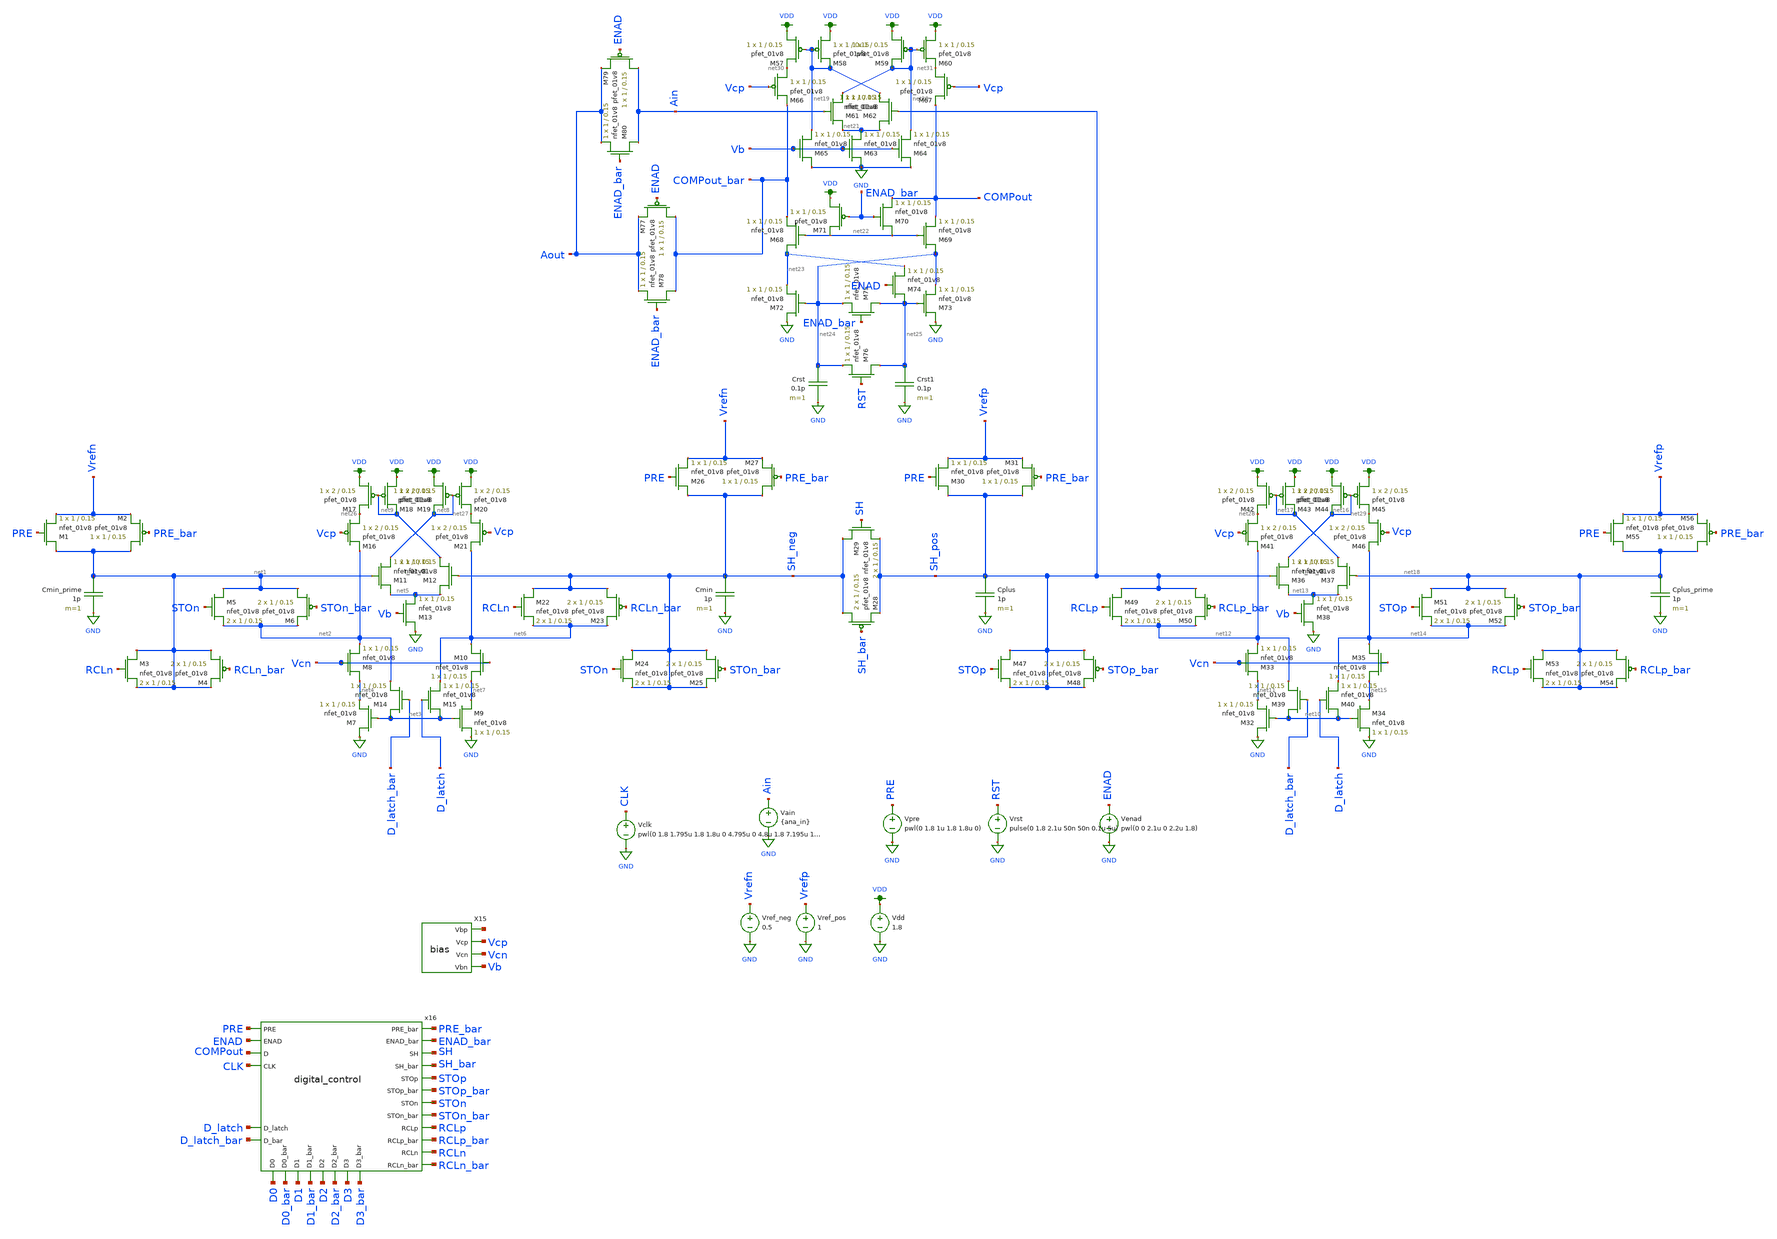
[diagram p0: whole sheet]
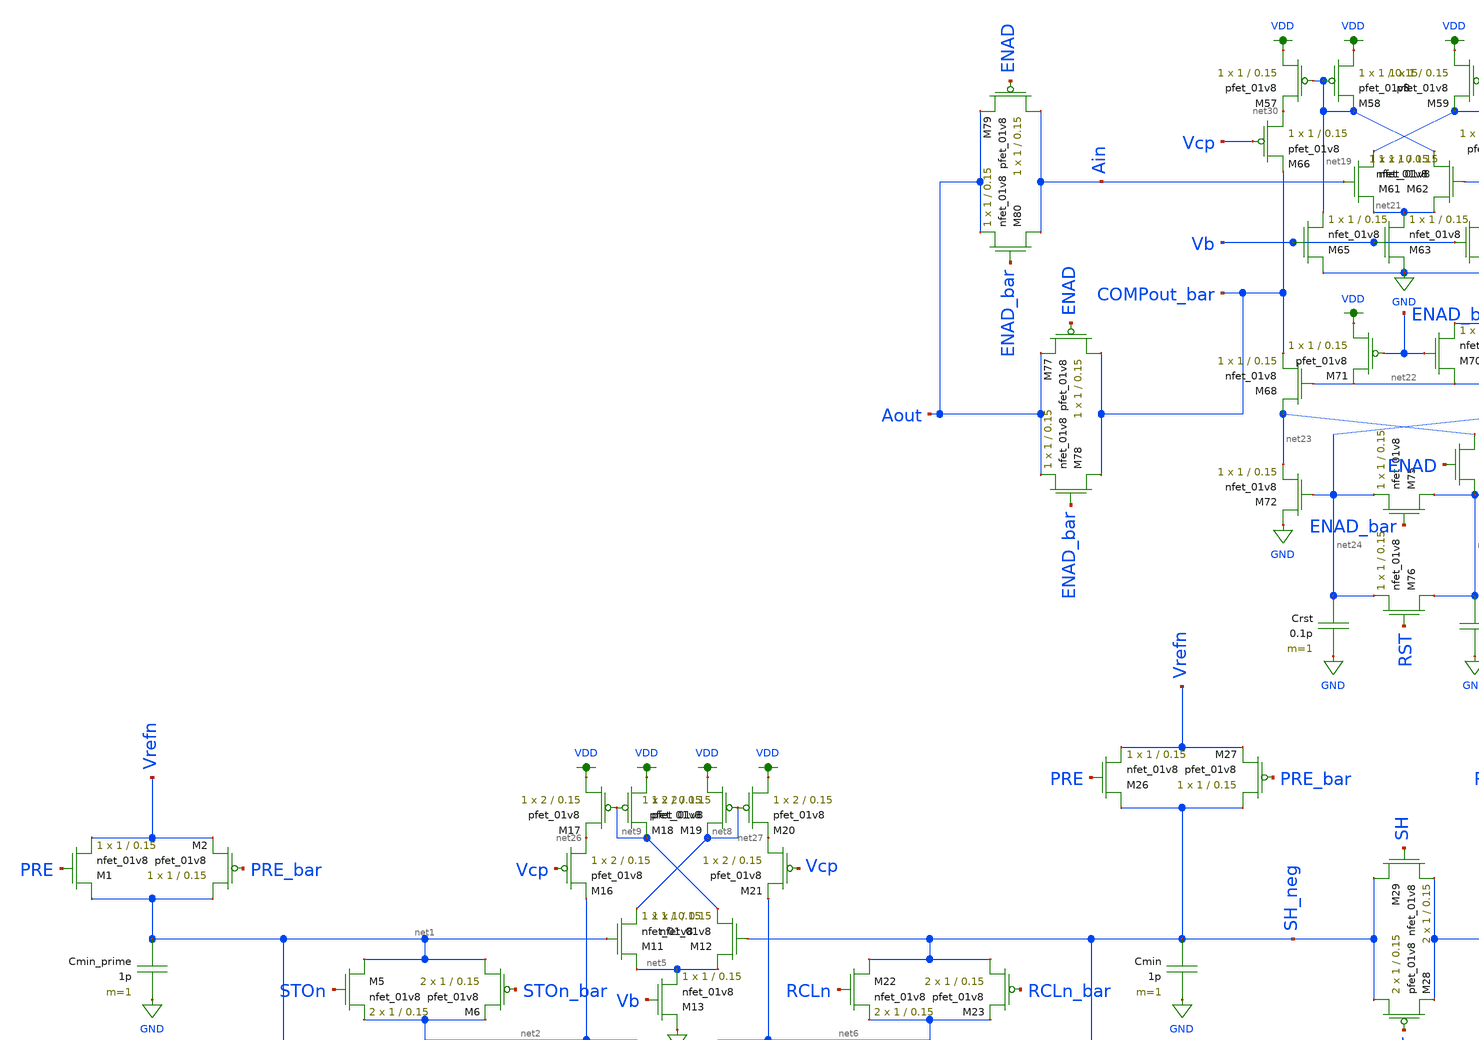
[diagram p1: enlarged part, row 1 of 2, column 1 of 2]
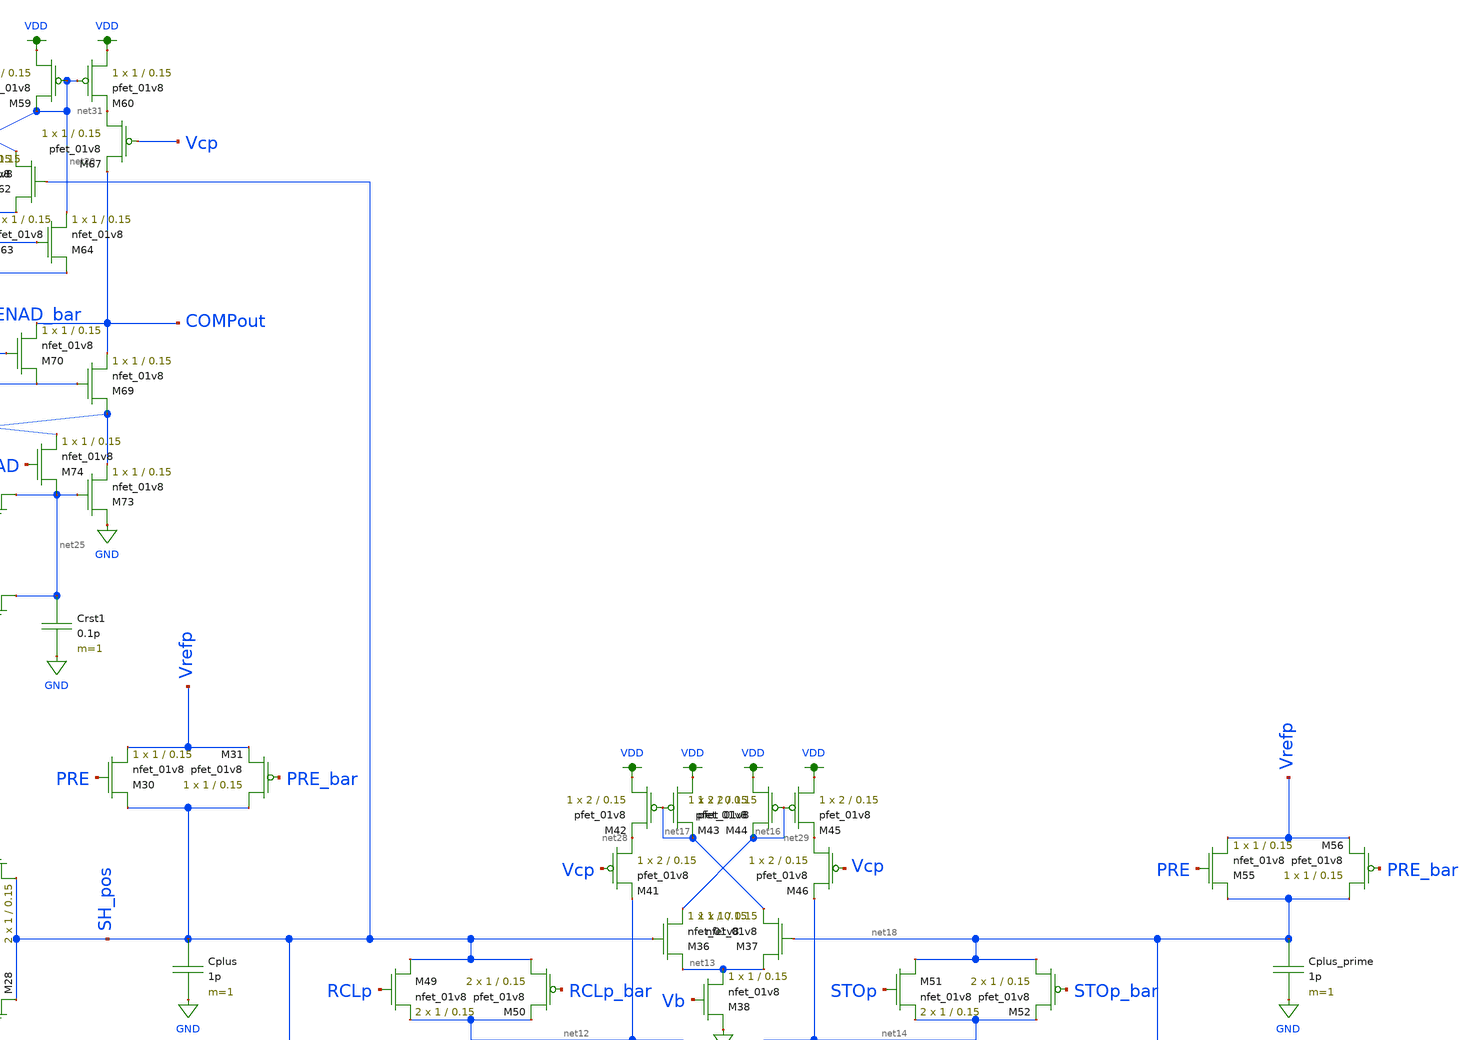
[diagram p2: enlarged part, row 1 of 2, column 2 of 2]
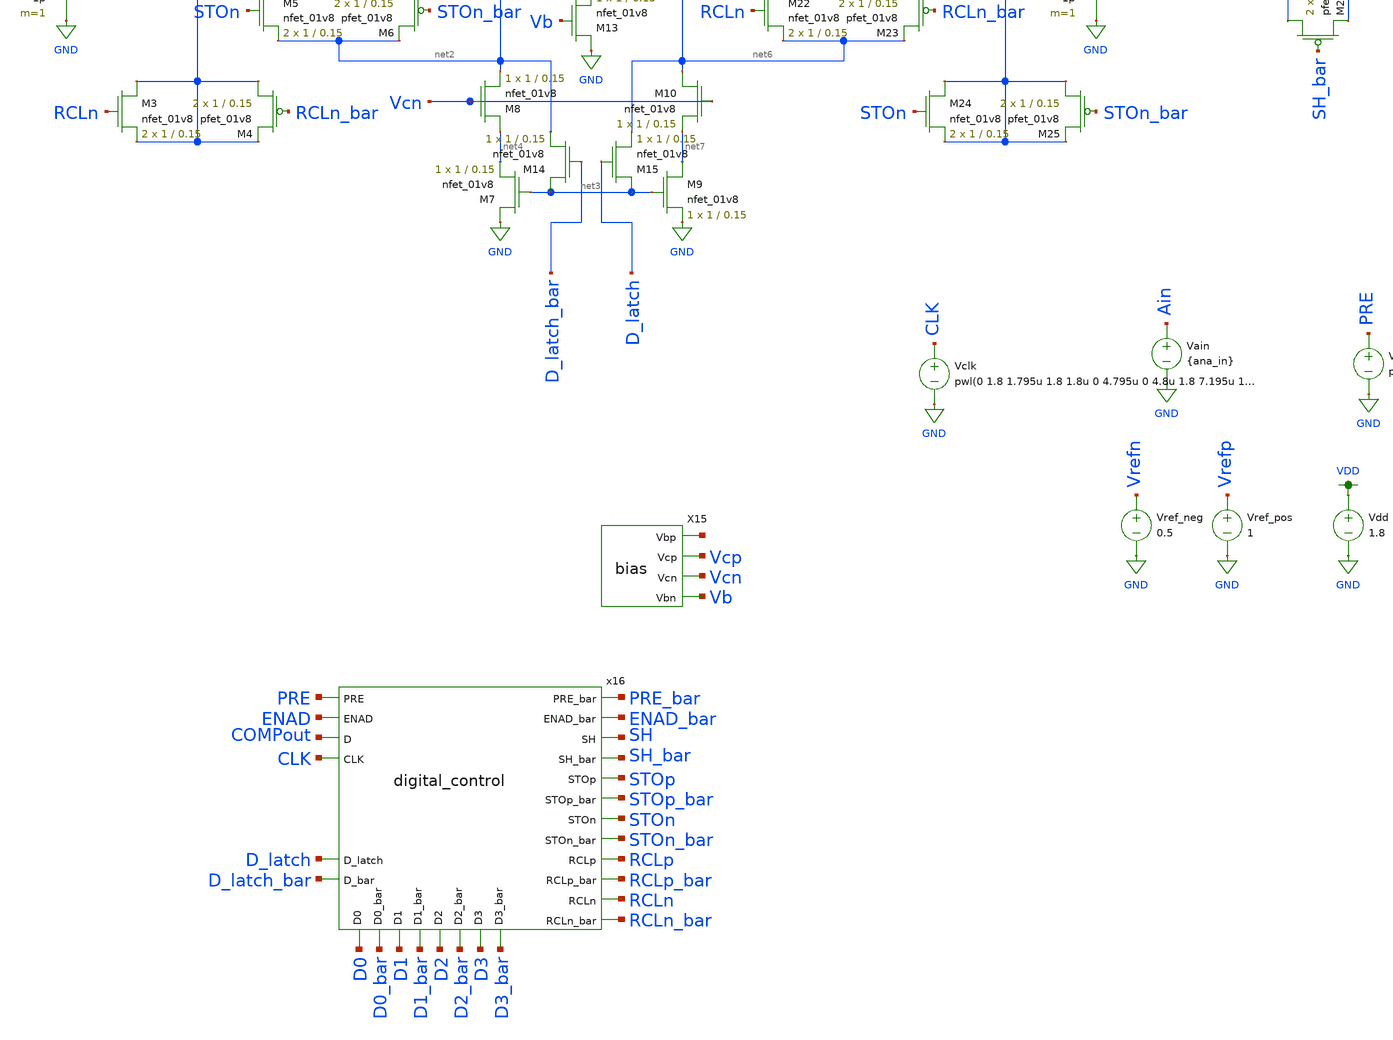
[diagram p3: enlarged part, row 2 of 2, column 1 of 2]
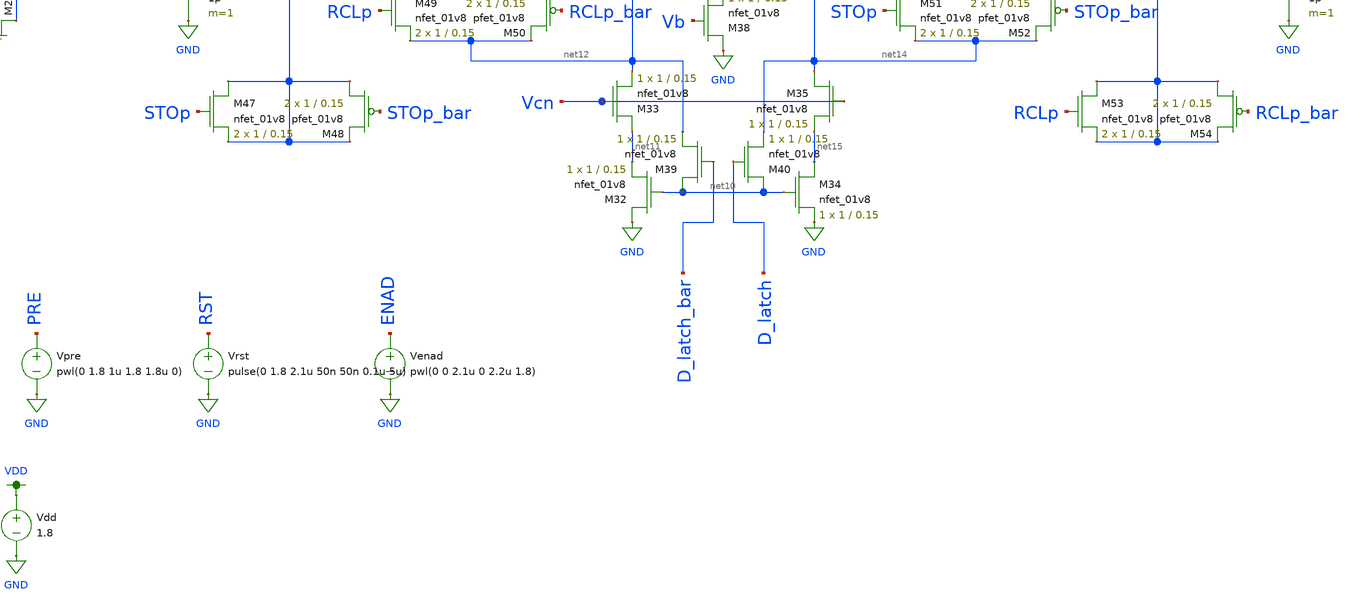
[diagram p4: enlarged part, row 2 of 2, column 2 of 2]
** sch_path: simulations/adc_mc.sch
**.subckt adc_mc
XM1 net1 PRE Vrefn GND sky130_fd_pr__nfet_01v8 L=0.15 W=1 nf=1 ad='int((nf+1)/2) * W/nf * 0.29' as='int((nf+2)/2) * W/nf * 0.29'
+ pd='2*int((nf+1)/2) * (W/nf + 0.29)' ps='2*int((nf+2)/2) * (W/nf + 0.29)' nrd='0.29 / W' nrs='0.29 / W'
+ sa=0 sb=0 sd=0 mult=1 m=1
XM2 net1 PRE_bar Vrefn VDD sky130_fd_pr__pfet_01v8 L=0.15 W=1 nf=1 ad='int((nf+1)/2) * W/nf * 0.29' as='int((nf+2)/2) * W/nf * 0.29'
+ pd='2*int((nf+1)/2) * (W/nf + 0.29)' ps='2*int((nf+2)/2) * (W/nf + 0.29)' nrd='0.29 / W' nrs='0.29 / W'
+ sa=0 sb=0 sd=0 mult=1 m=1
Cmin_prime net1 GND 1p m=1
XM3 net1 RCLn net1 GND sky130_fd_pr__nfet_01v8 L=0.15 W=1 nf=1 ad='int((nf+1)/2) * W/nf * 0.29' as='int((nf+2)/2) * W/nf * 0.29'
+ pd='2*int((nf+1)/2) * (W/nf + 0.29)' ps='2*int((nf+2)/2) * (W/nf + 0.29)' nrd='0.29 / W' nrs='0.29 / W'
+ sa=0 sb=0 sd=0 mult=2 m=2
XM4 net1 RCLn_bar net1 VDD sky130_fd_pr__pfet_01v8 L=0.15 W=1 nf=1 ad='int((nf+1)/2) * W/nf * 0.29' as='int((nf+2)/2) * W/nf * 0.29'
+ pd='2*int((nf+1)/2) * (W/nf + 0.29)' ps='2*int((nf+2)/2) * (W/nf + 0.29)' nrd='0.29 / W' nrs='0.29 / W'
+ sa=0 sb=0 sd=0 mult=2 m=2
XM5 net1 STOn net2 GND sky130_fd_pr__nfet_01v8 L=0.15 W=1 nf=1 ad='int((nf+1)/2) * W/nf * 0.29' as='int((nf+2)/2) * W/nf * 0.29'
+ pd='2*int((nf+1)/2) * (W/nf + 0.29)' ps='2*int((nf+2)/2) * (W/nf + 0.29)' nrd='0.29 / W' nrs='0.29 / W'
+ sa=0 sb=0 sd=0 mult=2 m=2
XM6 net1 STOn_bar net2 VDD sky130_fd_pr__pfet_01v8 L=0.15 W=1 nf=1 ad='int((nf+1)/2) * W/nf * 0.29' as='int((nf+2)/2) * W/nf * 0.29'
+ pd='2*int((nf+1)/2) * (W/nf + 0.29)' ps='2*int((nf+2)/2) * (W/nf + 0.29)' nrd='0.29 / W' nrs='0.29 / W'
+ sa=0 sb=0 sd=0 mult=2 m=2
XM7 GND net3 net4 GND sky130_fd_pr__nfet_01v8 L=0.15 W=1 nf=1 ad='int((nf+1)/2) * W/nf * 0.29' as='int((nf+2)/2) * W/nf * 0.29'
+ pd='2*int((nf+1)/2) * (W/nf + 0.29)' ps='2*int((nf+2)/2) * (W/nf + 0.29)' nrd='0.29 / W' nrs='0.29 / W'
+ sa=0 sb=0 sd=0 mult=1 m=1
XM8 net4 Vcn net2 GND sky130_fd_pr__nfet_01v8 L=0.15 W=1 nf=1 ad='int((nf+1)/2) * W/nf * 0.29' as='int((nf+2)/2) * W/nf * 0.29'
+ pd='2*int((nf+1)/2) * (W/nf + 0.29)' ps='2*int((nf+2)/2) * (W/nf + 0.29)' nrd='0.29 / W' nrs='0.29 / W'
+ sa=0 sb=0 sd=0 mult=1 m=1
XM9 net7 net3 GND GND sky130_fd_pr__nfet_01v8 L=0.15 W=1 nf=1 ad='int((nf+1)/2) * W/nf * 0.29' as='int((nf+2)/2) * W/nf * 0.29'
+ pd='2*int((nf+1)/2) * (W/nf + 0.29)' ps='2*int((nf+2)/2) * (W/nf + 0.29)' nrd='0.29 / W' nrs='0.29 / W'
+ sa=0 sb=0 sd=0 mult=1 m=1
XM10 net6 Vcn net7 GND sky130_fd_pr__nfet_01v8 L=0.15 W=1 nf=1 ad='int((nf+1)/2) * W/nf * 0.29' as='int((nf+2)/2) * W/nf * 0.29'
+ pd='2*int((nf+1)/2) * (W/nf + 0.29)' ps='2*int((nf+2)/2) * (W/nf + 0.29)' nrd='0.29 / W' nrs='0.29 / W'
+ sa=0 sb=0 sd=0 mult=1 m=1
XM11 net5 net1 net8 GND sky130_fd_pr__nfet_01v8 L=0.15 W=1 nf=1 ad='int((nf+1)/2) * W/nf * 0.29' as='int((nf+2)/2) * W/nf * 0.29'
+ pd='2*int((nf+1)/2) * (W/nf + 0.29)' ps='2*int((nf+2)/2) * (W/nf + 0.29)' nrd='0.29 / W' nrs='0.29 / W'
+ sa=0 sb=0 sd=0 mult=1 m=1
XM12 net5 SH_neg net9 GND sky130_fd_pr__nfet_01v8 L=0.15 W=1 nf=1 ad='int((nf+1)/2) * W/nf * 0.29' as='int((nf+2)/2) * W/nf * 0.29'
+ pd='2*int((nf+1)/2) * (W/nf + 0.29)' ps='2*int((nf+2)/2) * (W/nf + 0.29)' nrd='0.29 / W' nrs='0.29 / W'
+ sa=0 sb=0 sd=0 mult=1 m=1
XM13 GND Vb net5 GND sky130_fd_pr__nfet_01v8 L=0.15 W=1 nf=1 ad='int((nf+1)/2) * W/nf * 0.29' as='int((nf+2)/2) * W/nf * 0.29'
+ pd='2*int((nf+1)/2) * (W/nf + 0.29)' ps='2*int((nf+2)/2) * (W/nf + 0.29)' nrd='0.29 / W' nrs='0.29 / W'
+ sa=0 sb=0 sd=0 mult=1 m=1
XM14 net3 D_latch_bar net2 GND sky130_fd_pr__nfet_01v8 L=0.15 W=1 nf=1 ad='int((nf+1)/2) * W/nf * 0.29'
+ as='int((nf+2)/2) * W/nf * 0.29' pd='2*int((nf+1)/2) * (W/nf + 0.29)' ps='2*int((nf+2)/2) * (W/nf + 0.29)'
+ nrd='0.29 / W' nrs='0.29 / W' sa=0 sb=0 sd=0 mult=1 m=1
XM15 net3 D_latch net6 GND sky130_fd_pr__nfet_01v8 L=0.15 W=1 nf=1 ad='int((nf+1)/2) * W/nf * 0.29' as='int((nf+2)/2) * W/nf * 0.29'
+ pd='2*int((nf+1)/2) * (W/nf + 0.29)' ps='2*int((nf+2)/2) * (W/nf + 0.29)' nrd='0.29 / W' nrs='0.29 / W'
+ sa=0 sb=0 sd=0 mult=1 m=1
XM16 net26 Vcp net2 VDD sky130_fd_pr__pfet_01v8 L=0.15 W=2 nf=1 ad='int((nf+1)/2) * W/nf * 0.29' as='int((nf+2)/2) * W/nf * 0.29'
+ pd='2*int((nf+1)/2) * (W/nf + 0.29)' ps='2*int((nf+2)/2) * (W/nf + 0.29)' nrd='0.29 / W' nrs='0.29 / W'
+ sa=0 sb=0 sd=0 mult=1 m=1
XM17 VDD net9 net26 VDD sky130_fd_pr__pfet_01v8 L=0.15 W=2 nf=1 ad='int((nf+1)/2) * W/nf * 0.29' as='int((nf+2)/2) * W/nf * 0.29'
+ pd='2*int((nf+1)/2) * (W/nf + 0.29)' ps='2*int((nf+2)/2) * (W/nf + 0.29)' nrd='0.29 / W' nrs='0.29 / W'
+ sa=0 sb=0 sd=0 mult=1 m=1
XM18 VDD net9 net9 VDD sky130_fd_pr__pfet_01v8 L=0.15 W=2 nf=1 ad='int((nf+1)/2) * W/nf * 0.29' as='int((nf+2)/2) * W/nf * 0.29'
+ pd='2*int((nf+1)/2) * (W/nf + 0.29)' ps='2*int((nf+2)/2) * (W/nf + 0.29)' nrd='0.29 / W' nrs='0.29 / W'
+ sa=0 sb=0 sd=0 mult=1 m=1
XM19 VDD net8 net8 VDD sky130_fd_pr__pfet_01v8 L=0.15 W=2 nf=1 ad='int((nf+1)/2) * W/nf * 0.29' as='int((nf+2)/2) * W/nf * 0.29'
+ pd='2*int((nf+1)/2) * (W/nf + 0.29)' ps='2*int((nf+2)/2) * (W/nf + 0.29)' nrd='0.29 / W' nrs='0.29 / W'
+ sa=0 sb=0 sd=0 mult=1 m=1
XM20 VDD net8 net27 VDD sky130_fd_pr__pfet_01v8 L=0.15 W=2 nf=1 ad='int((nf+1)/2) * W/nf * 0.29' as='int((nf+2)/2) * W/nf * 0.29'
+ pd='2*int((nf+1)/2) * (W/nf + 0.29)' ps='2*int((nf+2)/2) * (W/nf + 0.29)' nrd='0.29 / W' nrs='0.29 / W'
+ sa=0 sb=0 sd=0 mult=1 m=1
XM21 net27 Vcp net6 VDD sky130_fd_pr__pfet_01v8 L=0.15 W=2 nf=1 ad='int((nf+1)/2) * W/nf * 0.29' as='int((nf+2)/2) * W/nf * 0.29'
+ pd='2*int((nf+1)/2) * (W/nf + 0.29)' ps='2*int((nf+2)/2) * (W/nf + 0.29)' nrd='0.29 / W' nrs='0.29 / W'
+ sa=0 sb=0 sd=0 mult=1 m=1
XM22 SH_neg RCLn net6 GND sky130_fd_pr__nfet_01v8 L=0.15 W=1 nf=1 ad='int((nf+1)/2) * W/nf * 0.29' as='int((nf+2)/2) * W/nf * 0.29'
+ pd='2*int((nf+1)/2) * (W/nf + 0.29)' ps='2*int((nf+2)/2) * (W/nf + 0.29)' nrd='0.29 / W' nrs='0.29 / W'
+ sa=0 sb=0 sd=0 mult=2 m=2
XM23 SH_neg RCLn_bar net6 VDD sky130_fd_pr__pfet_01v8 L=0.15 W=1 nf=1 ad='int((nf+1)/2) * W/nf * 0.29'
+ as='int((nf+2)/2) * W/nf * 0.29' pd='2*int((nf+1)/2) * (W/nf + 0.29)' ps='2*int((nf+2)/2) * (W/nf + 0.29)'
+ nrd='0.29 / W' nrs='0.29 / W' sa=0 sb=0 sd=0 mult=2 m=2
XM24 SH_neg STOn SH_neg GND sky130_fd_pr__nfet_01v8 L=0.15 W=1 nf=1 ad='int((nf+1)/2) * W/nf * 0.29'
+ as='int((nf+2)/2) * W/nf * 0.29' pd='2*int((nf+1)/2) * (W/nf + 0.29)' ps='2*int((nf+2)/2) * (W/nf + 0.29)'
+ nrd='0.29 / W' nrs='0.29 / W' sa=0 sb=0 sd=0 mult=2 m=2
XM25 SH_neg STOn_bar SH_neg VDD sky130_fd_pr__pfet_01v8 L=0.15 W=1 nf=1 ad='int((nf+1)/2) * W/nf * 0.29'
+ as='int((nf+2)/2) * W/nf * 0.29' pd='2*int((nf+1)/2) * (W/nf + 0.29)' ps='2*int((nf+2)/2) * (W/nf + 0.29)'
+ nrd='0.29 / W' nrs='0.29 / W' sa=0 sb=0 sd=0 mult=2 m=2
XM26 SH_neg PRE Vrefn GND sky130_fd_pr__nfet_01v8 L=0.15 W=1 nf=1 ad='int((nf+1)/2) * W/nf * 0.29' as='int((nf+2)/2) * W/nf * 0.29'
+ pd='2*int((nf+1)/2) * (W/nf + 0.29)' ps='2*int((nf+2)/2) * (W/nf + 0.29)' nrd='0.29 / W' nrs='0.29 / W'
+ sa=0 sb=0 sd=0 mult=1 m=1
XM27 SH_neg PRE_bar Vrefn VDD sky130_fd_pr__pfet_01v8 L=0.15 W=1 nf=1 ad='int((nf+1)/2) * W/nf * 0.29'
+ as='int((nf+2)/2) * W/nf * 0.29' pd='2*int((nf+1)/2) * (W/nf + 0.29)' ps='2*int((nf+2)/2) * (W/nf + 0.29)'
+ nrd='0.29 / W' nrs='0.29 / W' sa=0 sb=0 sd=0 mult=1 m=1
Cmin SH_neg GND 1p m=1
XM28 SH_neg SH_bar SH_pos VDD sky130_fd_pr__pfet_01v8 L=0.15 W=1 nf=1 ad='int((nf+1)/2) * W/nf * 0.29'
+ as='int((nf+2)/2) * W/nf * 0.29' pd='2*int((nf+1)/2) * (W/nf + 0.29)' ps='2*int((nf+2)/2) * (W/nf + 0.29)'
+ nrd='0.29 / W' nrs='0.29 / W' sa=0 sb=0 sd=0 mult=2 m=2
XM29 SH_neg SH SH_pos GND sky130_fd_pr__nfet_01v8 L=0.15 W=1 nf=1 ad='int((nf+1)/2) * W/nf * 0.29' as='int((nf+2)/2) * W/nf * 0.29'
+ pd='2*int((nf+1)/2) * (W/nf + 0.29)' ps='2*int((nf+2)/2) * (W/nf + 0.29)' nrd='0.29 / W' nrs='0.29 / W'
+ sa=0 sb=0 sd=0 mult=2 m=2
XM30 SH_pos PRE Vrefp GND sky130_fd_pr__nfet_01v8 L=0.15 W=1 nf=1 ad='int((nf+1)/2) * W/nf * 0.29' as='int((nf+2)/2) * W/nf * 0.29'
+ pd='2*int((nf+1)/2) * (W/nf + 0.29)' ps='2*int((nf+2)/2) * (W/nf + 0.29)' nrd='0.29 / W' nrs='0.29 / W'
+ sa=0 sb=0 sd=0 mult=1 m=1
XM31 SH_pos PRE_bar Vrefp VDD sky130_fd_pr__pfet_01v8 L=0.15 W=1 nf=1 ad='int((nf+1)/2) * W/nf * 0.29'
+ as='int((nf+2)/2) * W/nf * 0.29' pd='2*int((nf+1)/2) * (W/nf + 0.29)' ps='2*int((nf+2)/2) * (W/nf + 0.29)'
+ nrd='0.29 / W' nrs='0.29 / W' sa=0 sb=0 sd=0 mult=1 m=1
Cplus SH_pos GND 1p m=1
XM32 GND net10 net11 GND sky130_fd_pr__nfet_01v8 L=0.15 W=1 nf=1 ad='int((nf+1)/2) * W/nf * 0.29' as='int((nf+2)/2) * W/nf * 0.29'
+ pd='2*int((nf+1)/2) * (W/nf + 0.29)' ps='2*int((nf+2)/2) * (W/nf + 0.29)' nrd='0.29 / W' nrs='0.29 / W'
+ sa=0 sb=0 sd=0 mult=1 m=1
XM33 net11 Vcn net12 GND sky130_fd_pr__nfet_01v8 L=0.15 W=1 nf=1 ad='int((nf+1)/2) * W/nf * 0.29' as='int((nf+2)/2) * W/nf * 0.29'
+ pd='2*int((nf+1)/2) * (W/nf + 0.29)' ps='2*int((nf+2)/2) * (W/nf + 0.29)' nrd='0.29 / W' nrs='0.29 / W'
+ sa=0 sb=0 sd=0 mult=1 m=1
XM34 net15 net10 GND GND sky130_fd_pr__nfet_01v8 L=0.15 W=1 nf=1 ad='int((nf+1)/2) * W/nf * 0.29' as='int((nf+2)/2) * W/nf * 0.29'
+ pd='2*int((nf+1)/2) * (W/nf + 0.29)' ps='2*int((nf+2)/2) * (W/nf + 0.29)' nrd='0.29 / W' nrs='0.29 / W'
+ sa=0 sb=0 sd=0 mult=1 m=1
XM35 net14 Vcn net15 GND sky130_fd_pr__nfet_01v8 L=0.15 W=1 nf=1 ad='int((nf+1)/2) * W/nf * 0.29' as='int((nf+2)/2) * W/nf * 0.29'
+ pd='2*int((nf+1)/2) * (W/nf + 0.29)' ps='2*int((nf+2)/2) * (W/nf + 0.29)' nrd='0.29 / W' nrs='0.29 / W'
+ sa=0 sb=0 sd=0 mult=1 m=1
XM36 net13 SH_pos net16 GND sky130_fd_pr__nfet_01v8 L=0.15 W=1 nf=1 ad='int((nf+1)/2) * W/nf * 0.29'
+ as='int((nf+2)/2) * W/nf * 0.29' pd='2*int((nf+1)/2) * (W/nf + 0.29)' ps='2*int((nf+2)/2) * (W/nf + 0.29)'
+ nrd='0.29 / W' nrs='0.29 / W' sa=0 sb=0 sd=0 mult=1 m=1
XM37 net13 net18 net17 GND sky130_fd_pr__nfet_01v8 L=0.15 W=1 nf=1 ad='int((nf+1)/2) * W/nf * 0.29' as='int((nf+2)/2) * W/nf * 0.29'
+ pd='2*int((nf+1)/2) * (W/nf + 0.29)' ps='2*int((nf+2)/2) * (W/nf + 0.29)' nrd='0.29 / W' nrs='0.29 / W'
+ sa=0 sb=0 sd=0 mult=1 m=1
XM38 GND Vb net13 GND sky130_fd_pr__nfet_01v8 L=0.15 W=1 nf=1 ad='int((nf+1)/2) * W/nf * 0.29' as='int((nf+2)/2) * W/nf * 0.29'
+ pd='2*int((nf+1)/2) * (W/nf + 0.29)' ps='2*int((nf+2)/2) * (W/nf + 0.29)' nrd='0.29 / W' nrs='0.29 / W'
+ sa=0 sb=0 sd=0 mult=1 m=1
XM39 net10 D_latch_bar net12 GND sky130_fd_pr__nfet_01v8 L=0.15 W=1 nf=1 ad='int((nf+1)/2) * W/nf * 0.29'
+ as='int((nf+2)/2) * W/nf * 0.29' pd='2*int((nf+1)/2) * (W/nf + 0.29)' ps='2*int((nf+2)/2) * (W/nf + 0.29)'
+ nrd='0.29 / W' nrs='0.29 / W' sa=0 sb=0 sd=0 mult=1 m=1
XM40 net10 D_latch net14 GND sky130_fd_pr__nfet_01v8 L=0.15 W=1 nf=1 ad='int((nf+1)/2) * W/nf * 0.29'
+ as='int((nf+2)/2) * W/nf * 0.29' pd='2*int((nf+1)/2) * (W/nf + 0.29)' ps='2*int((nf+2)/2) * (W/nf + 0.29)'
+ nrd='0.29 / W' nrs='0.29 / W' sa=0 sb=0 sd=0 mult=1 m=1
XM41 net28 Vcp net12 VDD sky130_fd_pr__pfet_01v8 L=0.15 W=2 nf=1 ad='int((nf+1)/2) * W/nf * 0.29' as='int((nf+2)/2) * W/nf * 0.29'
+ pd='2*int((nf+1)/2) * (W/nf + 0.29)' ps='2*int((nf+2)/2) * (W/nf + 0.29)' nrd='0.29 / W' nrs='0.29 / W'
+ sa=0 sb=0 sd=0 mult=1 m=1
XM42 VDD net17 net28 VDD sky130_fd_pr__pfet_01v8 L=0.15 W=2 nf=1 ad='int((nf+1)/2) * W/nf * 0.29' as='int((nf+2)/2) * W/nf * 0.29'
+ pd='2*int((nf+1)/2) * (W/nf + 0.29)' ps='2*int((nf+2)/2) * (W/nf + 0.29)' nrd='0.29 / W' nrs='0.29 / W'
+ sa=0 sb=0 sd=0 mult=1 m=1
XM43 VDD net17 net17 VDD sky130_fd_pr__pfet_01v8 L=0.15 W=2 nf=1 ad='int((nf+1)/2) * W/nf * 0.29' as='int((nf+2)/2) * W/nf * 0.29'
+ pd='2*int((nf+1)/2) * (W/nf + 0.29)' ps='2*int((nf+2)/2) * (W/nf + 0.29)' nrd='0.29 / W' nrs='0.29 / W'
+ sa=0 sb=0 sd=0 mult=1 m=1
XM44 VDD net16 net16 VDD sky130_fd_pr__pfet_01v8 L=0.15 W=2 nf=1 ad='int((nf+1)/2) * W/nf * 0.29' as='int((nf+2)/2) * W/nf * 0.29'
+ pd='2*int((nf+1)/2) * (W/nf + 0.29)' ps='2*int((nf+2)/2) * (W/nf + 0.29)' nrd='0.29 / W' nrs='0.29 / W'
+ sa=0 sb=0 sd=0 mult=1 m=1
XM45 VDD net16 net29 VDD sky130_fd_pr__pfet_01v8 L=0.15 W=2 nf=1 ad='int((nf+1)/2) * W/nf * 0.29' as='int((nf+2)/2) * W/nf * 0.29'
+ pd='2*int((nf+1)/2) * (W/nf + 0.29)' ps='2*int((nf+2)/2) * (W/nf + 0.29)' nrd='0.29 / W' nrs='0.29 / W'
+ sa=0 sb=0 sd=0 mult=1 m=1
XM46 net29 Vcp net14 VDD sky130_fd_pr__pfet_01v8 L=0.15 W=2 nf=1 ad='int((nf+1)/2) * W/nf * 0.29' as='int((nf+2)/2) * W/nf * 0.29'
+ pd='2*int((nf+1)/2) * (W/nf + 0.29)' ps='2*int((nf+2)/2) * (W/nf + 0.29)' nrd='0.29 / W' nrs='0.29 / W'
+ sa=0 sb=0 sd=0 mult=1 m=1
XM47 SH_pos STOp SH_pos GND sky130_fd_pr__nfet_01v8 L=0.15 W=1 nf=1 ad='int((nf+1)/2) * W/nf * 0.29'
+ as='int((nf+2)/2) * W/nf * 0.29' pd='2*int((nf+1)/2) * (W/nf + 0.29)' ps='2*int((nf+2)/2) * (W/nf + 0.29)'
+ nrd='0.29 / W' nrs='0.29 / W' sa=0 sb=0 sd=0 mult=2 m=2
XM48 SH_pos STOp_bar SH_pos VDD sky130_fd_pr__pfet_01v8 L=0.15 W=1 nf=1 ad='int((nf+1)/2) * W/nf * 0.29'
+ as='int((nf+2)/2) * W/nf * 0.29' pd='2*int((nf+1)/2) * (W/nf + 0.29)' ps='2*int((nf+2)/2) * (W/nf + 0.29)'
+ nrd='0.29 / W' nrs='0.29 / W' sa=0 sb=0 sd=0 mult=2 m=2
XM49 SH_pos RCLp net12 GND sky130_fd_pr__nfet_01v8 L=0.15 W=1 nf=1 ad='int((nf+1)/2) * W/nf * 0.29' as='int((nf+2)/2) * W/nf * 0.29'
+ pd='2*int((nf+1)/2) * (W/nf + 0.29)' ps='2*int((nf+2)/2) * (W/nf + 0.29)' nrd='0.29 / W' nrs='0.29 / W'
+ sa=0 sb=0 sd=0 mult=2 m=2
XM50 SH_pos RCLp_bar net12 VDD sky130_fd_pr__pfet_01v8 L=0.15 W=1 nf=1 ad='int((nf+1)/2) * W/nf * 0.29'
+ as='int((nf+2)/2) * W/nf * 0.29' pd='2*int((nf+1)/2) * (W/nf + 0.29)' ps='2*int((nf+2)/2) * (W/nf + 0.29)'
+ nrd='0.29 / W' nrs='0.29 / W' sa=0 sb=0 sd=0 mult=2 m=2
XM51 net18 STOp net14 GND sky130_fd_pr__nfet_01v8 L=0.15 W=1 nf=1 ad='int((nf+1)/2) * W/nf * 0.29' as='int((nf+2)/2) * W/nf * 0.29'
+ pd='2*int((nf+1)/2) * (W/nf + 0.29)' ps='2*int((nf+2)/2) * (W/nf + 0.29)' nrd='0.29 / W' nrs='0.29 / W'
+ sa=0 sb=0 sd=0 mult=2 m=2
XM52 net18 STOp_bar net14 VDD sky130_fd_pr__pfet_01v8 L=0.15 W=1 nf=1 ad='int((nf+1)/2) * W/nf * 0.29'
+ as='int((nf+2)/2) * W/nf * 0.29' pd='2*int((nf+1)/2) * (W/nf + 0.29)' ps='2*int((nf+2)/2) * (W/nf + 0.29)'
+ nrd='0.29 / W' nrs='0.29 / W' sa=0 sb=0 sd=0 mult=2 m=2
XM53 net18 RCLp net18 GND sky130_fd_pr__nfet_01v8 L=0.15 W=1 nf=1 ad='int((nf+1)/2) * W/nf * 0.29' as='int((nf+2)/2) * W/nf * 0.29'
+ pd='2*int((nf+1)/2) * (W/nf + 0.29)' ps='2*int((nf+2)/2) * (W/nf + 0.29)' nrd='0.29 / W' nrs='0.29 / W'
+ sa=0 sb=0 sd=0 mult=2 m=2
XM54 net18 RCLp_bar net18 VDD sky130_fd_pr__pfet_01v8 L=0.15 W=1 nf=1 ad='int((nf+1)/2) * W/nf * 0.29'
+ as='int((nf+2)/2) * W/nf * 0.29' pd='2*int((nf+1)/2) * (W/nf + 0.29)' ps='2*int((nf+2)/2) * (W/nf + 0.29)'
+ nrd='0.29 / W' nrs='0.29 / W' sa=0 sb=0 sd=0 mult=2 m=2
XM55 net18 PRE Vrefp GND sky130_fd_pr__nfet_01v8 L=0.15 W=1 nf=1 ad='int((nf+1)/2) * W/nf * 0.29' as='int((nf+2)/2) * W/nf * 0.29'
+ pd='2*int((nf+1)/2) * (W/nf + 0.29)' ps='2*int((nf+2)/2) * (W/nf + 0.29)' nrd='0.29 / W' nrs='0.29 / W'
+ sa=0 sb=0 sd=0 mult=1 m=1
XM56 net18 PRE_bar Vrefp VDD sky130_fd_pr__pfet_01v8 L=0.15 W=1 nf=1 ad='int((nf+1)/2) * W/nf * 0.29'
+ as='int((nf+2)/2) * W/nf * 0.29' pd='2*int((nf+1)/2) * (W/nf + 0.29)' ps='2*int((nf+2)/2) * (W/nf + 0.29)'
+ nrd='0.29 / W' nrs='0.29 / W' sa=0 sb=0 sd=0 mult=1 m=1
Cplus_prime net18 GND 1p m=1
XM57 VDD net19 net30 VDD sky130_fd_pr__pfet_01v8 L=0.15 W=1 nf=1 ad='int((nf+1)/2) * W/nf * 0.29' as='int((nf+2)/2) * W/nf * 0.29'
+ pd='2*int((nf+1)/2) * (W/nf + 0.29)' ps='2*int((nf+2)/2) * (W/nf + 0.29)' nrd='0.29 / W' nrs='0.29 / W'
+ sa=0 sb=0 sd=0 mult=1 m=1
XM58 VDD net19 net19 VDD sky130_fd_pr__pfet_01v8 L=0.15 W=1 nf=1 ad='int((nf+1)/2) * W/nf * 0.29' as='int((nf+2)/2) * W/nf * 0.29'
+ pd='2*int((nf+1)/2) * (W/nf + 0.29)' ps='2*int((nf+2)/2) * (W/nf + 0.29)' nrd='0.29 / W' nrs='0.29 / W'
+ sa=0 sb=0 sd=0 mult=1 m=1
XM59 VDD net20 net20 VDD sky130_fd_pr__pfet_01v8 L=0.15 W=1 nf=1 ad='int((nf+1)/2) * W/nf * 0.29' as='int((nf+2)/2) * W/nf * 0.29'
+ pd='2*int((nf+1)/2) * (W/nf + 0.29)' ps='2*int((nf+2)/2) * (W/nf + 0.29)' nrd='0.29 / W' nrs='0.29 / W'
+ sa=0 sb=0 sd=0 mult=1 m=1
XM60 VDD net20 net31 VDD sky130_fd_pr__pfet_01v8 L=0.15 W=1 nf=1 ad='int((nf+1)/2) * W/nf * 0.29' as='int((nf+2)/2) * W/nf * 0.29'
+ pd='2*int((nf+1)/2) * (W/nf + 0.29)' ps='2*int((nf+2)/2) * (W/nf + 0.29)' nrd='0.29 / W' nrs='0.29 / W'
+ sa=0 sb=0 sd=0 mult=1 m=1
XM61 net21 Ain net20 GND sky130_fd_pr__nfet_01v8 L=0.15 W=1 nf=1 ad='int((nf+1)/2) * W/nf * 0.29' as='int((nf+2)/2) * W/nf * 0.29'
+ pd='2*int((nf+1)/2) * (W/nf + 0.29)' ps='2*int((nf+2)/2) * (W/nf + 0.29)' nrd='0.29 / W' nrs='0.29 / W'
+ sa=0 sb=0 sd=0 mult=1 m=1
XM62 net21 SH_pos net19 GND sky130_fd_pr__nfet_01v8 L=0.15 W=1 nf=1 ad='int((nf+1)/2) * W/nf * 0.29'
+ as='int((nf+2)/2) * W/nf * 0.29' pd='2*int((nf+1)/2) * (W/nf + 0.29)' ps='2*int((nf+2)/2) * (W/nf + 0.29)'
+ nrd='0.29 / W' nrs='0.29 / W' sa=0 sb=0 sd=0 mult=1 m=1
XM63 GND Vb net21 GND sky130_fd_pr__nfet_01v8 L=0.15 W=1 nf=1 ad='int((nf+1)/2) * W/nf * 0.29' as='int((nf+2)/2) * W/nf * 0.29'
+ pd='2*int((nf+1)/2) * (W/nf + 0.29)' ps='2*int((nf+2)/2) * (W/nf + 0.29)' nrd='0.29 / W' nrs='0.29 / W'
+ sa=0 sb=0 sd=0 mult=1 m=1
XM64 GND Vb net20 GND sky130_fd_pr__nfet_01v8 L=0.15 W=1 nf=1 ad='int((nf+1)/2) * W/nf * 0.29' as='int((nf+2)/2) * W/nf * 0.29'
+ pd='2*int((nf+1)/2) * (W/nf + 0.29)' ps='2*int((nf+2)/2) * (W/nf + 0.29)' nrd='0.29 / W' nrs='0.29 / W'
+ sa=0 sb=0 sd=0 mult=1 m=1
XM65 GND Vb net19 GND sky130_fd_pr__nfet_01v8 L=0.15 W=1 nf=1 ad='int((nf+1)/2) * W/nf * 0.29' as='int((nf+2)/2) * W/nf * 0.29'
+ pd='2*int((nf+1)/2) * (W/nf + 0.29)' ps='2*int((nf+2)/2) * (W/nf + 0.29)' nrd='0.29 / W' nrs='0.29 / W'
+ sa=0 sb=0 sd=0 mult=1 m=1
XM66 net30 Vcp COMPout_bar VDD sky130_fd_pr__pfet_01v8 L=0.15 W=1 nf=1 ad='int((nf+1)/2) * W/nf * 0.29'
+ as='int((nf+2)/2) * W/nf * 0.29' pd='2*int((nf+1)/2) * (W/nf + 0.29)' ps='2*int((nf+2)/2) * (W/nf + 0.29)'
+ nrd='0.29 / W' nrs='0.29 / W' sa=0 sb=0 sd=0 mult=1 m=1
XM67 net31 Vcp COMPout VDD sky130_fd_pr__pfet_01v8 L=0.15 W=1 nf=1 ad='int((nf+1)/2) * W/nf * 0.29' as='int((nf+2)/2) * W/nf * 0.29'
+ pd='2*int((nf+1)/2) * (W/nf + 0.29)' ps='2*int((nf+2)/2) * (W/nf + 0.29)' nrd='0.29 / W' nrs='0.29 / W'
+ sa=0 sb=0 sd=0 mult=1 m=1
XM68 net23 net22 COMPout_bar GND sky130_fd_pr__nfet_01v8 L=0.15 W=1 nf=1 ad='int((nf+1)/2) * W/nf * 0.29'
+ as='int((nf+2)/2) * W/nf * 0.29' pd='2*int((nf+1)/2) * (W/nf + 0.29)' ps='2*int((nf+2)/2) * (W/nf + 0.29)'
+ nrd='0.29 / W' nrs='0.29 / W' sa=0 sb=0 sd=0 mult=1 m=1
XM69 net24 net22 COMPout GND sky130_fd_pr__nfet_01v8 L=0.15 W=1 nf=1 ad='int((nf+1)/2) * W/nf * 0.29'
+ as='int((nf+2)/2) * W/nf * 0.29' pd='2*int((nf+1)/2) * (W/nf + 0.29)' ps='2*int((nf+2)/2) * (W/nf + 0.29)'
+ nrd='0.29 / W' nrs='0.29 / W' sa=0 sb=0 sd=0 mult=1 m=1
XM70 net22 ENAD_bar COMPout GND sky130_fd_pr__nfet_01v8 L=0.15 W=1 nf=1 ad='int((nf+1)/2) * W/nf * 0.29'
+ as='int((nf+2)/2) * W/nf * 0.29' pd='2*int((nf+1)/2) * (W/nf + 0.29)' ps='2*int((nf+2)/2) * (W/nf + 0.29)'
+ nrd='0.29 / W' nrs='0.29 / W' sa=0 sb=0 sd=0 mult=1 m=1
XM71 VDD ENAD_bar net22 VDD sky130_fd_pr__pfet_01v8 L=0.15 W=1 nf=1 ad='int((nf+1)/2) * W/nf * 0.29'
+ as='int((nf+2)/2) * W/nf * 0.29' pd='2*int((nf+1)/2) * (W/nf + 0.29)' ps='2*int((nf+2)/2) * (W/nf + 0.29)'
+ nrd='0.29 / W' nrs='0.29 / W' sa=0 sb=0 sd=0 mult=1 m=1
XM72 GND net24 net23 GND sky130_fd_pr__nfet_01v8 L=0.15 W=1 nf=1 ad='int((nf+1)/2) * W/nf * 0.29' as='int((nf+2)/2) * W/nf * 0.29'
+ pd='2*int((nf+1)/2) * (W/nf + 0.29)' ps='2*int((nf+2)/2) * (W/nf + 0.29)' nrd='0.29 / W' nrs='0.29 / W'
+ sa=0 sb=0 sd=0 mult=1 m=1
XM73 GND net25 net24 GND sky130_fd_pr__nfet_01v8 L=0.15 W=1 nf=1 ad='int((nf+1)/2) * W/nf * 0.29' as='int((nf+2)/2) * W/nf * 0.29'
+ pd='2*int((nf+1)/2) * (W/nf + 0.29)' ps='2*int((nf+2)/2) * (W/nf + 0.29)' nrd='0.29 / W' nrs='0.29 / W'
+ sa=0 sb=0 sd=0 mult=1 m=1
XM74 net25 ENAD net23 GND sky130_fd_pr__nfet_01v8 L=0.15 W=1 nf=1 ad='int((nf+1)/2) * W/nf * 0.29' as='int((nf+2)/2) * W/nf * 0.29'
+ pd='2*int((nf+1)/2) * (W/nf + 0.29)' ps='2*int((nf+2)/2) * (W/nf + 0.29)' nrd='0.29 / W' nrs='0.29 / W'
+ sa=0 sb=0 sd=0 mult=1 m=1
XM75 net25 ENAD_bar net24 GND sky130_fd_pr__nfet_01v8 L=0.15 W=1 nf=1 ad='int((nf+1)/2) * W/nf * 0.29'
+ as='int((nf+2)/2) * W/nf * 0.29' pd='2*int((nf+1)/2) * (W/nf + 0.29)' ps='2*int((nf+2)/2) * (W/nf + 0.29)'
+ nrd='0.29 / W' nrs='0.29 / W' sa=0 sb=0 sd=0 mult=1 m=1
Crst net24 GND 0.1p m=1
XM76 net25 RST net24 GND sky130_fd_pr__nfet_01v8 L=0.15 W=1 nf=1 ad='int((nf+1)/2) * W/nf * 0.29' as='int((nf+2)/2) * W/nf * 0.29'
+ pd='2*int((nf+1)/2) * (W/nf + 0.29)' ps='2*int((nf+2)/2) * (W/nf + 0.29)' nrd='0.29 / W' nrs='0.29 / W'
+ sa=0 sb=0 sd=0 mult=1 m=1
Crst1 net25 GND 0.1p m=1
XM77 COMPout_bar ENAD Aout VDD sky130_fd_pr__pfet_01v8 L=0.15 W=1 nf=1 ad='int((nf+1)/2) * W/nf * 0.29'
+ as='int((nf+2)/2) * W/nf * 0.29' pd='2*int((nf+1)/2) * (W/nf + 0.29)' ps='2*int((nf+2)/2) * (W/nf + 0.29)'
+ nrd='0.29 / W' nrs='0.29 / W' sa=0 sb=0 sd=0 mult=1 m=1
XM78 COMPout_bar ENAD_bar Aout GND sky130_fd_pr__nfet_01v8 L=0.15 W=1 nf=1 ad='int((nf+1)/2) * W/nf * 0.29'
+ as='int((nf+2)/2) * W/nf * 0.29' pd='2*int((nf+1)/2) * (W/nf + 0.29)' ps='2*int((nf+2)/2) * (W/nf + 0.29)'
+ nrd='0.29 / W' nrs='0.29 / W' sa=0 sb=0 sd=0 mult=1 m=1
XM79 Ain ENAD Aout VDD sky130_fd_pr__pfet_01v8 L=0.15 W=1 nf=1 ad='int((nf+1)/2) * W/nf * 0.29' as='int((nf+2)/2) * W/nf * 0.29'
+ pd='2*int((nf+1)/2) * (W/nf + 0.29)' ps='2*int((nf+2)/2) * (W/nf + 0.29)' nrd='0.29 / W' nrs='0.29 / W'
+ sa=0 sb=0 sd=0 mult=1 m=1
XM80 Ain ENAD_bar Aout GND sky130_fd_pr__nfet_01v8 L=0.15 W=1 nf=1 ad='int((nf+1)/2) * W/nf * 0.29' as='int((nf+2)/2) * W/nf * 0.29'
+ pd='2*int((nf+1)/2) * (W/nf + 0.29)' ps='2*int((nf+2)/2) * (W/nf + 0.29)' nrd='0.29 / W' nrs='0.29 / W'
+ sa=0 sb=0 sd=0 mult=1 m=1
Vclk CLK GND pwl(0 1.8 1.795u 1.8 1.8u 0 4.795u 0 4.8u 1.8 7.195u 1.8 7.2u 0 9.795u 0 9.8u 1.8
+ 12.195u 1.8 12.2u 0 14.795u 0 14.8u 1.8 17.195u 1.8 17.2u 0 19.795u 0 19.8u 1.8 22.195u 1.8 22.2u 0 24.795u
+ 0 24.8u 1.8 27.195u 1.8 27.2u 0)
Vrst RST GND pulse(0 1.8 2.1u 50n 50n 0.1u 5u)
Venad ENAD GND pwl(0 0 2.1u 0 2.2u 1.8)
Vref_neg Vrefn GND 0.5
Vref_pos Vrefp GND 1
Vain Ain GND {ana_in}
X15 net32 Vcp Vcn Vb bias
Vpre PRE GND pwl(0 1.8 1u 1.8 1.8u 0)
x16 STOn RCLn SH STOp RCLp SH_bar ENAD_bar PRE_bar PRE ENAD D0 COMPout D0_bar CLK STOp_bar STOn_bar
+ RCLp_bar RCLn_bar D1 D2 D3 D_latch_bar D_latch D1_bar D2_bar D3_bar digital_control
Vdd VDD GND 1.8
**** begin user architecture code

.option wnflag=1
.param MC_SWITCH=1.0
.lib ~/skywater/skywater-pdk/libraries/sky130_fd_pr_ngspice/latest/models/sky130.lib.spice tt


.ic v(D0)=0 v(D1)=0 v(D2)=0 v(D3)=0
.ic v(D0_bar)=1.8 v(D1_bar)=1.8 v(D2_bar)=1.8 v(D3_bar)=1.8
.param ana_in = 0
.control
  let runs = 10
  let run = 0
  while run <= runs
  set wr_vecnames
  set wr_singlescale
  let code=0
  while code < 16
    alterparam ana_in = {$&code*0.03125 + 0.515625}
    reset
    tran 1n 19.1u 5.9u
    wrdata ~/algorithmic-ada-converter/python/adc/adc{$&run}.txt v(Ain) v(COMPout)
    if code eq 0
      set appendwrite
      set wr_vecnames = FALSE
    end
    let code = code + 1
  end
  let run = run + 1
  reset
  end
.endc

**** end user architecture code
**.ends

* expanding   symbol:  ../schematics/bias.sym # of pins=4
** sym_path: schematics/bias.sym
** sch_path: schematics/bias.sch
.subckt bias Vbp Vcp Vcn Vbn
*.opin Vcp
*.opin Vcn
*.opin Vbn
*.opin Vbp
XM1 net1 Vbn GND GND sky130_fd_pr__nfet_01v8 L=2.5 W=12 nf=1 ad='int((nf+1)/2) * W/nf * 0.29' as='int((nf+2)/2) * W/nf * 0.29'
+ pd='2*int((nf+1)/2) * (W/nf + 0.29)' ps='2*int((nf+2)/2) * (W/nf + 0.29)' nrd='0.29 / W' nrs='0.29 / W'
+ sa=0 sb=0 sd=0 mult=1 m=1
XM2 Vcp Vbn GND GND sky130_fd_pr__nfet_01v8 L=0.5 W=12 nf=1 ad='int((nf+1)/2) * W/nf * 0.29' as='int((nf+2)/2) * W/nf * 0.29'
+ pd='2*int((nf+1)/2) * (W/nf + 0.29)' ps='2*int((nf+2)/2) * (W/nf + 0.29)' nrd='0.29 / W' nrs='0.29 / W'
+ sa=0 sb=0 sd=0 mult=1 m=1
XM3 Vbp Vbn GND GND sky130_fd_pr__nfet_01v8 L=0.5 W=12 nf=1 ad='int((nf+1)/2) * W/nf * 0.29' as='int((nf+2)/2) * W/nf * 0.29'
+ pd='2*int((nf+1)/2) * (W/nf + 0.29)' ps='2*int((nf+2)/2) * (W/nf + 0.29)' nrd='0.29 / W' nrs='0.29 / W'
+ sa=0 sb=0 sd=0 mult=1 m=1
XM4 net3 net4 GND GND sky130_fd_pr__nfet_01v8 L=0.5 W=12 nf=1 ad='int((nf+1)/2) * W/nf * 0.29' as='int((nf+2)/2) * W/nf * 0.29'
+ pd='2*int((nf+1)/2) * (W/nf + 0.29)' ps='2*int((nf+2)/2) * (W/nf + 0.29)' nrd='0.29 / W' nrs='0.29 / W'
+ sa=0 sb=0 sd=0 mult=1 m=1
XM5 Vbn Vbn GND GND sky130_fd_pr__nfet_01v8 L=0.5 W=12 nf=1 ad='int((nf+1)/2) * W/nf * 0.29' as='int((nf+2)/2) * W/nf * 0.29'
+ pd='2*int((nf+1)/2) * (W/nf + 0.29)' ps='2*int((nf+2)/2) * (W/nf + 0.29)' nrd='0.29 / W' nrs='0.29 / W'
+ sa=0 sb=0 sd=0 mult=1 m=1
XM6 net4 net4 net3 GND sky130_fd_pr__nfet_01v8 L=0.5 W=48 nf=1 ad='int((nf+1)/2) * W/nf * 0.29' as='int((nf+2)/2) * W/nf * 0.29'
+ pd='2*int((nf+1)/2) * (W/nf + 0.29)' ps='2*int((nf+2)/2) * (W/nf + 0.29)' nrd='0.29 / W' nrs='0.29 / W'
+ sa=0 sb=0 sd=0 mult=1 m=1
XM7 Vcn Vcn net3 GND sky130_fd_pr__nfet_01v8 L=0.5 W=12 nf=1 ad='int((nf+1)/2) * W/nf * 0.29' as='int((nf+2)/2) * W/nf * 0.29'
+ pd='2*int((nf+1)/2) * (W/nf + 0.29)' ps='2*int((nf+2)/2) * (W/nf + 0.29)' nrd='0.29 / W' nrs='0.29 / W'
+ sa=0 sb=0 sd=0 mult=1 m=1
XM8 net1 net1 net2 VDD sky130_fd_pr__pfet_01v8 L=0.5 W=48 nf=1 ad='int((nf+1)/2) * W/nf * 0.29' as='int((nf+2)/2) * W/nf * 0.29'
+ pd='2*int((nf+1)/2) * (W/nf + 0.29)' ps='2*int((nf+2)/2) * (W/nf + 0.29)' nrd='0.29 / W' nrs='0.29 / W'
+ sa=0 sb=0 sd=0 mult=1 m=1
XM9 net2 net1 VDD VDD sky130_fd_pr__pfet_01v8 L=0.5 W=12 nf=1 ad='int((nf+1)/2) * W/nf * 0.29' as='int((nf+2)/2) * W/nf * 0.29'
+ pd='2*int((nf+1)/2) * (W/nf + 0.29)' ps='2*int((nf+2)/2) * (W/nf + 0.29)' nrd='0.29 / W' nrs='0.29 / W'
+ sa=0 sb=0 sd=0 mult=1 m=1
XM10 Vcp Vcp net2 VDD sky130_fd_pr__pfet_01v8 L=0.5 W=12 nf=1 ad='int((nf+1)/2) * W/nf * 0.29' as='int((nf+2)/2) * W/nf * 0.29'
+ pd='2*int((nf+1)/2) * (W/nf + 0.29)' ps='2*int((nf+2)/2) * (W/nf + 0.29)' nrd='0.29 / W' nrs='0.29 / W'
+ sa=0 sb=0 sd=0 mult=1 m=1
XM11 Vbp Vbp VDD VDD sky130_fd_pr__pfet_01v8 L=0.5 W=12 nf=1 ad='int((nf+1)/2) * W/nf * 0.29' as='int((nf+2)/2) * W/nf * 0.29'
+ pd='2*int((nf+1)/2) * (W/nf + 0.29)' ps='2*int((nf+2)/2) * (W/nf + 0.29)' nrd='0.29 / W' nrs='0.29 / W'
+ sa=0 sb=0 sd=0 mult=1 m=1
XM12 net4 Vbp VDD VDD sky130_fd_pr__pfet_01v8 L=2.5 W=12 nf=1 ad='int((nf+1)/2) * W/nf * 0.29' as='int((nf+2)/2) * W/nf * 0.29'
+ pd='2*int((nf+1)/2) * (W/nf + 0.29)' ps='2*int((nf+2)/2) * (W/nf + 0.29)' nrd='0.29 / W' nrs='0.29 / W'
+ sa=0 sb=0 sd=0 mult=1 m=1
XM13 Vcn Vbp VDD VDD sky130_fd_pr__pfet_01v8 L=0.5 W=12 nf=1 ad='int((nf+1)/2) * W/nf * 0.29' as='int((nf+2)/2) * W/nf * 0.29'
+ pd='2*int((nf+1)/2) * (W/nf + 0.29)' ps='2*int((nf+2)/2) * (W/nf + 0.29)' nrd='0.29 / W' nrs='0.29 / W'
+ sa=0 sb=0 sd=0 mult=1 m=1
I1 VDD Vbn 100u
.ends


* expanding   symbol:  /home/madvlsi/algorithmic-ada-converter/schematics/digital_control.sym # of
*+ pins=26
** sym_path: schematics/digital_control.sym
** sch_path: schematics/digital_control.sch
.subckt digital_control STOn RCLn SH STOp RCLp SH_bar ENAD_bar PRE_bar PRE ENAD D0 D D0_bar CLK
+ STOp_bar STOn_bar RCLp_bar RCLn_bar D1 D2 D3 D_bar D_latch D1_bar D2_bar D3_bar
*.ipin D
*.opin D1
*.opin D2
*.opin D3
*.ipin CLK
*.opin SH_bar
*.opin SH
*.ipin PRE
*.opin PRE_bar
*.ipin ENAD
*.opin ENAD_bar
*.opin STOp
*.opin STOn
*.opin RCLp
*.opin RCLn
*.opin D0_bar
*.opin STOn_bar
*.opin STOp_bar
*.opin RCLn_bar
*.opin RCLp_bar
*.opin D0
*.opin D_bar
*.opin D_latch
*.opin D1_bar
*.opin D2_bar
*.opin D3_bar
x4 CLK D1 D0 D1_bar D0_bar CRSL_edge_sens
x5 CLK D2 D1 D2_bar D1_bar CRSL_edge_sens
x6 CLK D3 D2 D3_bar D2_bar CRSL_edge_sens
x10 VDD CLK STOn_bar D GND nand2
X13 STOn_bar STOn VDD GND inverter
X16 RCLn_bar RCLn VDD GND inverter
X17 STOp_bar STOp VDD GND inverter
X18 RCLp_bar RCLp VDD GND inverter
x19 VDD CLK RCLn_bar D_bar GND nand2
x20 VDD CLK STOp_bar D_bar GND nand2
x21 VDD CLK RCLp_bar D GND nand2
X23 D D_bar VDD GND inverter
X12 CLK SH VDD GND inverter
X1 SH SH_bar VDD GND inverter
X11 PRE PRE_bar VDD GND inverter
X14 ENAD ENAD_bar VDD GND inverter
x2 CLK D0 D_latch D0_bar D_bar CRSL_edge_sens
X3 D_bar D_latch VDD GND inverter
.ends


* expanding   symbol:  ../schematics/CRSL_edge_sens.sym # of pins=5
** sym_path: schematics/CRSL_edge_sens.sym
** sch_path: schematics/CRSL_edge_sens.sch
.subckt CRSL_edge_sens Phi Q D Q_bar D_bar
*.ipin D
*.ipin D_bar
*.opin Q
*.opin Q_bar
*.ipin Phi
XM14 Q_bar Q GND GND sky130_fd_pr__nfet_01v8 L=0.15 W=1 nf=1 ad='int((nf+1)/2) * W/nf * 0.29' as='int((nf+2)/2) * W/nf * 0.29'
+ pd='2*int((nf+1)/2) * (W/nf + 0.29)' ps='2*int((nf+2)/2) * (W/nf + 0.29)' nrd='0.29 / W' nrs='0.29 / W'
+ sa=0 sb=0 sd=0 mult=1 m=1
XM2 Q_bar Phi net3 GND sky130_fd_pr__nfet_01v8 L=0.15 W=1 nf=1 ad='int((nf+1)/2) * W/nf * 0.29' as='int((nf+2)/2) * W/nf * 0.29'
+ pd='2*int((nf+1)/2) * (W/nf + 0.29)' ps='2*int((nf+2)/2) * (W/nf + 0.29)' nrd='0.29 / W' nrs='0.29 / W'
+ sa=0 sb=0 sd=0 mult=1 m=1
XM6 Q Phi net2 GND sky130_fd_pr__nfet_01v8 L=0.15 W=1 nf=1 ad='int((nf+1)/2) * W/nf * 0.29' as='int((nf+2)/2) * W/nf * 0.29'
+ pd='2*int((nf+1)/2) * (W/nf + 0.29)' ps='2*int((nf+2)/2) * (W/nf + 0.29)' nrd='0.29 / W' nrs='0.29 / W'
+ sa=0 sb=0 sd=0 mult=1 m=1
XM7 net4 Phi GND GND sky130_fd_pr__nfet_01v8 L=0.15 W=4 nf=1 ad='int((nf+1)/2) * W/nf * 0.29' as='int((nf+2)/2) * W/nf * 0.29'
+ pd='2*int((nf+1)/2) * (W/nf + 0.29)' ps='2*int((nf+2)/2) * (W/nf + 0.29)' nrd='0.29 / W' nrs='0.29 / W'
+ sa=0 sb=0 sd=0 mult=1 m=1
XM8 net3 net2 net4 GND sky130_fd_pr__nfet_01v8 L=0.15 W=1 nf=1 ad='int((nf+1)/2) * W/nf * 0.29' as='int((nf+2)/2) * W/nf * 0.29'
+ pd='2*int((nf+1)/2) * (W/nf + 0.29)' ps='2*int((nf+2)/2) * (W/nf + 0.29)' nrd='0.29 / W' nrs='0.29 / W'
+ sa=0 sb=0 sd=0 mult=1 m=1
XM12 net3 net2 VDD VDD sky130_fd_pr__pfet_01v8 L=0.15 W=1 nf=1 ad='int((nf+1)/2) * W/nf * 0.29' as='int((nf+2)/2) * W/nf * 0.29'
+ pd='2*int((nf+1)/2) * (W/nf + 0.29)' ps='2*int((nf+2)/2) * (W/nf + 0.29)' nrd='0.29 / W' nrs='0.29 / W'
+ sa=0 sb=0 sd=0 mult=1 m=1
XM9 net2 net3 VDD VDD sky130_fd_pr__pfet_01v8 L=0.15 W=1 nf=1 ad='int((nf+1)/2) * W/nf * 0.29' as='int((nf+2)/2) * W/nf * 0.29'
+ pd='2*int((nf+1)/2) * (W/nf + 0.29)' ps='2*int((nf+2)/2) * (W/nf + 0.29)' nrd='0.29 / W' nrs='0.29 / W'
+ sa=0 sb=0 sd=0 mult=1 m=1
XM1 net1 Phi VDD VDD sky130_fd_pr__pfet_01v8 L=0.15 W=8 nf=1 ad='int((nf+1)/2) * W/nf * 0.29' as='int((nf+2)/2) * W/nf * 0.29'
+ pd='2*int((nf+1)/2) * (W/nf + 0.29)' ps='2*int((nf+2)/2) * (W/nf + 0.29)' nrd='0.29 / W' nrs='0.29 / W'
+ sa=0 sb=0 sd=0 mult=1 m=1
XM3 Q_bar Q net1 VDD sky130_fd_pr__pfet_01v8 L=0.15 W=1 nf=1 ad='int((nf+1)/2) * W/nf * 0.29' as='int((nf+2)/2) * W/nf * 0.29'
+ pd='2*int((nf+1)/2) * (W/nf + 0.29)' ps='2*int((nf+2)/2) * (W/nf + 0.29)' nrd='0.29 / W' nrs='0.29 / W'
+ sa=0 sb=0 sd=0 mult=1 m=1
XM4 Q Q_bar net1 VDD sky130_fd_pr__pfet_01v8 L=0.15 W=1 nf=1 ad='int((nf+1)/2) * W/nf * 0.29' as='int((nf+2)/2) * W/nf * 0.29'
+ pd='2*int((nf+1)/2) * (W/nf + 0.29)' ps='2*int((nf+2)/2) * (W/nf + 0.29)' nrd='0.29 / W' nrs='0.29 / W'
+ sa=0 sb=0 sd=0 mult=1 m=1
XM10 Q Q_bar GND GND sky130_fd_pr__nfet_01v8 L=0.15 W=1 nf=1 ad='int((nf+1)/2) * W/nf * 0.29' as='int((nf+2)/2) * W/nf * 0.29'
+ pd='2*int((nf+1)/2) * (W/nf + 0.29)' ps='2*int((nf+2)/2) * (W/nf + 0.29)' nrd='0.29 / W' nrs='0.29 / W'
+ sa=0 sb=0 sd=0 mult=1 m=1
XM5 net2 net3 net4 GND sky130_fd_pr__nfet_01v8 L=0.15 W=1 nf=1 ad='int((nf+1)/2) * W/nf * 0.29' as='int((nf+2)/2) * W/nf * 0.29'
+ pd='2*int((nf+1)/2) * (W/nf + 0.29)' ps='2*int((nf+2)/2) * (W/nf + 0.29)' nrd='0.29 / W' nrs='0.29 / W'
+ sa=0 sb=0 sd=0 mult=1 m=1
XM11 net3 Phi D_bar VDD sky130_fd_pr__pfet_01v8 L=0.15 W=1 nf=1 ad='int((nf+1)/2) * W/nf * 0.29' as='int((nf+2)/2) * W/nf * 0.29'
+ pd='2*int((nf+1)/2) * (W/nf + 0.29)' ps='2*int((nf+2)/2) * (W/nf + 0.29)' nrd='0.29 / W' nrs='0.29 / W'
+ sa=0 sb=0 sd=0 mult=1 m=1
XM15 net2 Phi D VDD sky130_fd_pr__pfet_01v8 L=0.15 W=1 nf=1 ad='int((nf+1)/2) * W/nf * 0.29' as='int((nf+2)/2) * W/nf * 0.29'
+ pd='2*int((nf+1)/2) * (W/nf + 0.29)' ps='2*int((nf+2)/2) * (W/nf + 0.29)' nrd='0.29 / W' nrs='0.29 / W'
+ sa=0 sb=0 sd=0 mult=1 m=1
.ends


* expanding   symbol:  ../schematics/nand2.sym # of pins=5
** sym_path: schematics/nand2.sym
** sch_path: schematics/nand2.sch
.subckt nand2 VP B Y A VN
*.iopin VP
*.iopin VN
*.ipin A
*.ipin B
*.opin Y
XM5 Y B VP VP sky130_fd_pr__pfet_01v8 L=0.15 W=1 nf=1 ad='int((nf+1)/2) * W/nf * 0.29' as='int((nf+2)/2) * W/nf * 0.29'
+ pd='2*int((nf+1)/2) * (W/nf + 0.29)' ps='2*int((nf+2)/2) * (W/nf + 0.29)' nrd='0.29 / W' nrs='0.29 / W'
+ sa=0 sb=0 sd=0 mult=1 m=1
XM2 Y A VP VP sky130_fd_pr__pfet_01v8 L=0.15 W=1 nf=1 ad='int((nf+1)/2) * W/nf * 0.29' as='int((nf+2)/2) * W/nf * 0.29'
+ pd='2*int((nf+1)/2) * (W/nf + 0.29)' ps='2*int((nf+2)/2) * (W/nf + 0.29)' nrd='0.29 / W' nrs='0.29 / W'
+ sa=0 sb=0 sd=0 mult=1 m=1
XM1 Y A net1 VN sky130_fd_pr__nfet_01v8 L=0.15 W=1 nf=1 ad='int((nf+1)/2) * W/nf * 0.29' as='int((nf+2)/2) * W/nf * 0.29'
+ pd='2*int((nf+1)/2) * (W/nf + 0.29)' ps='2*int((nf+2)/2) * (W/nf + 0.29)' nrd='0.29 / W' nrs='0.29 / W'
+ sa=0 sb=0 sd=0 mult=1 m=1
XM3 net1 B VN VN sky130_fd_pr__nfet_01v8 L=0.15 W=1 nf=1 ad='int((nf+1)/2) * W/nf * 0.29' as='int((nf+2)/2) * W/nf * 0.29'
+ pd='2*int((nf+1)/2) * (W/nf + 0.29)' ps='2*int((nf+2)/2) * (W/nf + 0.29)' nrd='0.29 / W' nrs='0.29 / W'
+ sa=0 sb=0 sd=0 mult=1 m=1
.ends


* expanding   symbol:  ../schematics/inverter.sym # of pins=4
** sym_path: schematics/inverter.sym
** sch_path: schematics/inverter.sch
.subckt inverter A Y VP VN
*.ipin A
*.iopin VP
*.iopin VN
*.opin Y
XM1 Y A VP VDD sky130_fd_pr__pfet_01v8 L=0.15 W=1 nf=1 ad='int((nf+1)/2) * W/nf * 0.29' as='int((nf+2)/2) * W/nf * 0.29'
+ pd='2*int((nf+1)/2) * (W/nf + 0.29)' ps='2*int((nf+2)/2) * (W/nf + 0.29)' nrd='0.29 / W' nrs='0.29 / W'
+ sa=0 sb=0 sd=0 mult=1 m=1
XM2 Y A VN GND sky130_fd_pr__nfet_01v8 L=0.15 W=1 nf=1 ad='int((nf+1)/2) * W/nf * 0.29' as='int((nf+2)/2) * W/nf * 0.29'
+ pd='2*int((nf+1)/2) * (W/nf + 0.29)' ps='2*int((nf+2)/2) * (W/nf + 0.29)' nrd='0.29 / W' nrs='0.29 / W'
+ sa=0 sb=0 sd=0 mult=1 m=1
.ends

.GLOBAL GND
.GLOBAL VDD
.end
